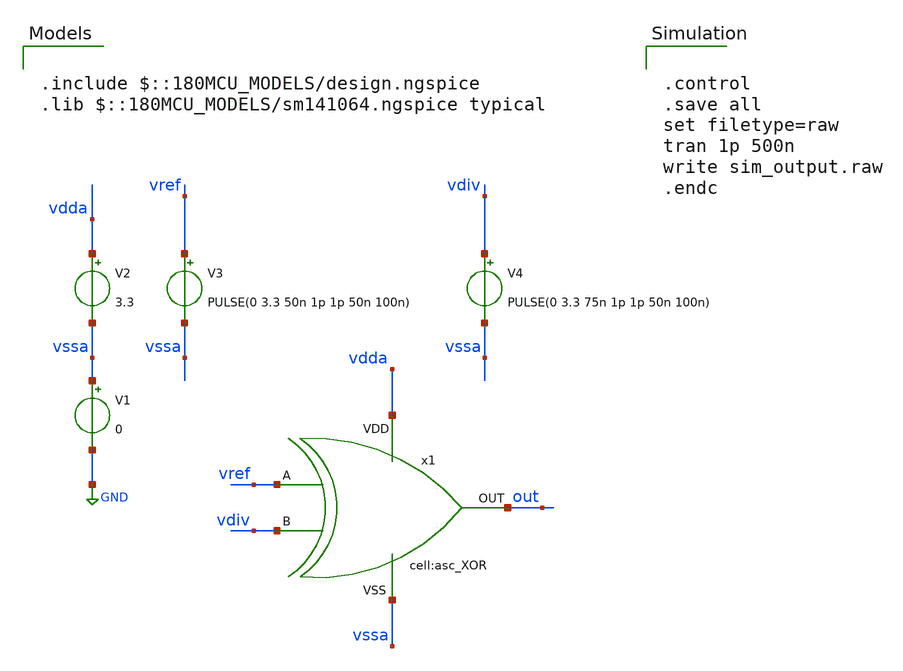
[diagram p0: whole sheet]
** sch_path: designs/libs/tb_analog/tb_asc_PFD_XOR/tb_asc_PFD_XOR.sch
**.subckt tb_asc_PFD_XOR
V1 vssa GND 0
V2 vdda vssa 3.3
V3 vref vssa PULSE(0 3.3 50n 1p 1p 50n 100n)
V4 vdiv vssa PULSE(0 3.3 75n 1p 1p 50n 100n)
x1 vdda vssa out vref vdiv asc_XOR
**** begin user architecture code

.include $::180MCU_MODELS/design.ngspice
.lib $::180MCU_MODELS/sm141064.ngspice typical



.control
.save all
set filetype=raw
tran 1p 500n
write sim_output.raw
.endc


**** end user architecture code
**.ends
.GLOBAL GND
.end
